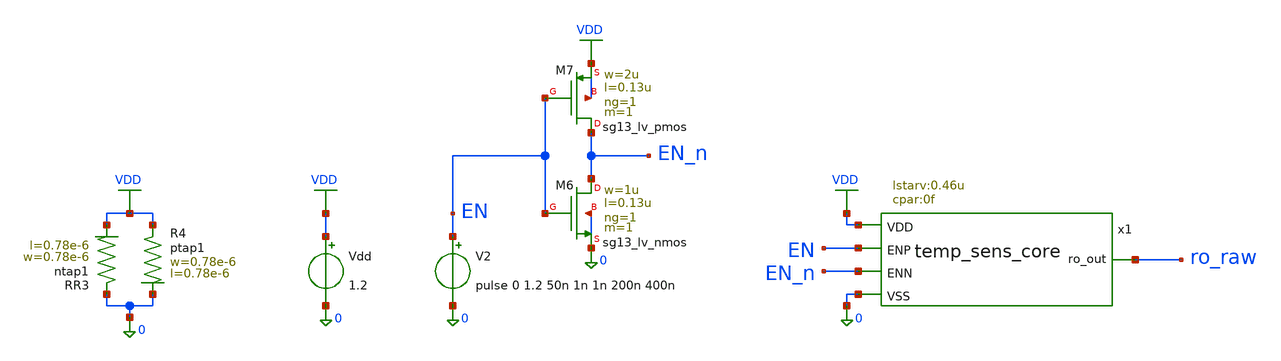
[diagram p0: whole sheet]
** sch_path: analog/temp-sens-core/testbenches/temp-sens-core_temp-sweep.sch
**.subckt temp-sens-core_temp-sweep
Vdd VDD 0 1.2
XR3 0 VDD ntap1 R=262.8 w=0.78e-6 l=0.78e-6
XR4 VDD 0 ptap1 R=262.8 w=0.78e-6 l=0.78e-6
x1 EN EN_n ro_raw VDD 0 temp_sens_core
XM6 EN_n EN 0 0 sg13_lv_nmos w=1u l=0.13u ng=1 m=1 mm_ok=1
XM7 EN_n EN VDD VDD sg13_lv_pmos w=2u l=0.13u ng=1 m=1 mm_ok=1
V2 EN 0 pulse 0 1.2 50n 1n 1n 200n 400n
**** begin user architecture code



* ngspice commands
.option rshunt=1e12
.option klu
*.param cpar=0
*.param lstarv=0.18u
.control
set num_threads = 8

let temp_start = -20
let temp_stop = 140
let temp_delta = 10

* Create one plot that will hold the sweep results
setplot new
set scratch = $curplot

compose temperature start=$&temp_start stop=$&temp_stop step=$&temp_delta
let frequency = vector(length(temperature))

let i = 0
let tcur = temp_start
while tcur <= temp_stop
  option temp = $&tcur

  tran 0.05n 300n

  meas tran tperiod
  + TRIG v(ro_raw) VAL=0.6 RISE=2 TD=75n
  + TARG v(ro_raw) VAL=0.6 RISE=3 TD=75n

  * Remember the just-created tran plot
  set dt = $curplot

  * Go back to the scratch plot before touching loop variables
  setplot $scratch

  if tcur = 20
    write temp-sens-core_temp-sweep_temp25_wave.raw {$dt}.time {$dt}.v(ro_raw) {$dt}.en {$dt}.en_n
*    let time25 = {$dt}.time
*    let ro_raw25 = {$dt}.v(ro_raw)
  end

  let frequency[i] = 1/{$dt}.tperiod

  let tcur = tcur + temp_delta
  let i = i+1
end

setplot $scratch

settype temp-sweep temperature
settype frequency frequency
setscale frequency temperature
write temp-sens-core_temp-sweep.raw temperature frequency
.endc






.lib cornerMOSlv.lib mos_tt
.lib cornerMOShv.lib mos_tt
.lib cornerRES.lib res_typ
.lib cornerDIO.lib dio_tt






.include /foss/pdks/ihp-sg13cmos5l/libs.ref/sg13cmos5l_stdcell/spice/sg13cmos5l_stdcell.spice



**** end user architecture code
**.ends

* expanding   symbol:  analog/temp-sens-core/temp_sens_core.sym # of pins=5
** sym_path: analog/temp-sens-core/temp_sens_core.sym
** sch_path: analog/temp-sens-core/temp_sens_core.sch
.subckt temp_sens_core ENP ENN ro_out VDD VSS  lstarv=0.13u cpar=0
*.opin ro_out
*.iopin VDD
*.iopin VSS
*.ipin ENP
*.ipin ENN
XM1 net1 vgp VDD VDD sg13_lv_pmos w=1.5u l={lstarv} ng=1 m=1 mm_ok=1
XM21 vgp ENP VDD VDD sg13_lv_pmos w=10u l=0.13u ng=1 m=1 mm_ok=1
XM22 vgn ENN VSS VSS sg13_lv_nmos w=10u l=0.13u ng=1 m=1 mm_ok=1
XM23 vgp vgp VDD VDD sg13_lv_pmos w=1.5u l={lstarv} ng=1 m=1 mm_ok=1
XM24 vgn vgn VSS VSS sg13_lv_nmos w=1.5u l={lstarv} ng=1 m=1 mm_ok=1
XM4 net8 vgn VSS VSS sg13_lv_nmos w=1.5u l={lstarv} ng=1 m=1 mm_ok=1
XM5 net2 vgp VDD VDD sg13_lv_pmos w=1.5u l={lstarv} ng=1 m=1 mm_ok=1
XM8 net11 vgn VSS VSS sg13_lv_nmos w=1.5u l={lstarv} ng=1 m=1 mm_ok=1
XM9 net3 vgp VDD VDD sg13_lv_pmos w=1.5u l={lstarv} ng=1 m=1 mm_ok=1
XM12 net13 vgn VSS VSS sg13_lv_nmos w=1.5u l={lstarv} ng=1 m=1 mm_ok=1
XM13 net4 vgp VDD VDD sg13_lv_pmos w=1.5u l={lstarv} ng=1 m=1 mm_ok=1
XM16 net15 vgn VSS VSS sg13_lv_nmos w=1.5u l={lstarv} ng=1 m=1 mm_ok=1
XM17 net5 vgp VDD VDD sg13_lv_pmos w=1.5u l={lstarv} ng=1 m=1 mm_ok=1
XM20 net16 vgn VSS VSS sg13_lv_nmos w=1.5u l={lstarv} ng=1 m=1 mm_ok=1
XM25 net6 vgp VDD VDD sg13_lv_pmos w=1.5u l={lstarv} ng=1 m=1 mm_ok=1
XM28 net18 vgn VSS VSS sg13_lv_nmos w=1.5u l={lstarv} ng=1 m=1 mm_ok=1
XM29 net7 vgp VDD VDD sg13_lv_pmos w=1.5u l={lstarv} ng=1 m=1 mm_ok=1
XM32 net19 vgn VSS VSS sg13_lv_nmos w=1.5u l={lstarv} ng=1 m=1 mm_ok=1
x1 net1 ro_out net9 net8 inverter
x2 net2 net9 net10 net11 inverter
x3 net3 net10 net12 net13 inverter
x4 net4 net12 net14 net15 inverter
x5 net5 net14 net22 net16 inverter
x6 net6 net22 net17 net18 inverter
x7 net7 net17 net28 net19 inverter
XM2 VSS net20 vgp VSS sg13_lv_pmos w=1u l=0.13u ng=1 m=1 mm_ok=1
XM3 VDD net21 vgn VDD sg13_lv_nmos w=1u l=0.13u ng=1 m=1 mm_ok=1
XR6 VDD net20 sub! rsil w=0.5e-6 l=75e-6 m=1 mm_ok=1
XR7 net20 VSS sub! rsil w=0.5e-6 l=10e-6 m=1 mm_ok=1
XR1 net21 VSS sub! rsil w=0.5e-6 l=75e-6 m=1 mm_ok=1
XR2 VDD net21 sub! rsil w=0.5e-6 l=10e-6 m=1 mm_ok=1
C1 net9 VSS {cpar} m=1
C2 net10 VSS {cpar} m=1
C3 net12 VSS {cpar} m=1
C4 net14 VSS {cpar} m=1
C5 net22 VSS {cpar} m=1
C6 net17 VSS {cpar} m=1
C7 net28 VSS {cpar} m=1
XM6 net23 vgp VDD VDD sg13_lv_pmos w=1.5u l={lstarv} ng=1 m=1 mm_ok=1
XM7 net26 vgn VSS VSS sg13_lv_nmos w=1.5u l={lstarv} ng=1 m=1 mm_ok=1
XM10 net24 vgp VDD VDD sg13_lv_pmos w=1.5u l={lstarv} ng=1 m=1 mm_ok=1
XM11 net27 vgn VSS VSS sg13_lv_nmos w=1.5u l={lstarv} ng=1 m=1 mm_ok=1
x8 net23 net28 net25 net26 inverter
x9 net24 net25 ro_out net27 inverter
C8 net25 VSS {cpar} m=1
C9 ro_out VSS {cpar} m=1
**** begin user architecture code



.include /foss/pdks/ihp-sg13cmos5l/libs.ref/sg13cmos5l_stdcell/spice/sg13cmos5l_stdcell.spice



**** end user architecture code
.ends


* expanding   symbol:  analog/inverter/inverter.sym # of pins=4
** sym_path: analog/inverter/inverter.sym
** sch_path: analog/inverter/inverter.sch
.subckt inverter pos in out neg
*.ipin in
*.iopin pos
*.iopin neg
*.opin out
XM1 out in neg neg sg13_lv_nmos w=2.0u l=0.45u ng=1 m=1 mm_ok=1
XM2 pos in out pos sg13_lv_pmos w=1.0u l=0.45u ng=1 m=1 mm_ok=1
.ends

.GLOBAL VDD
.end
